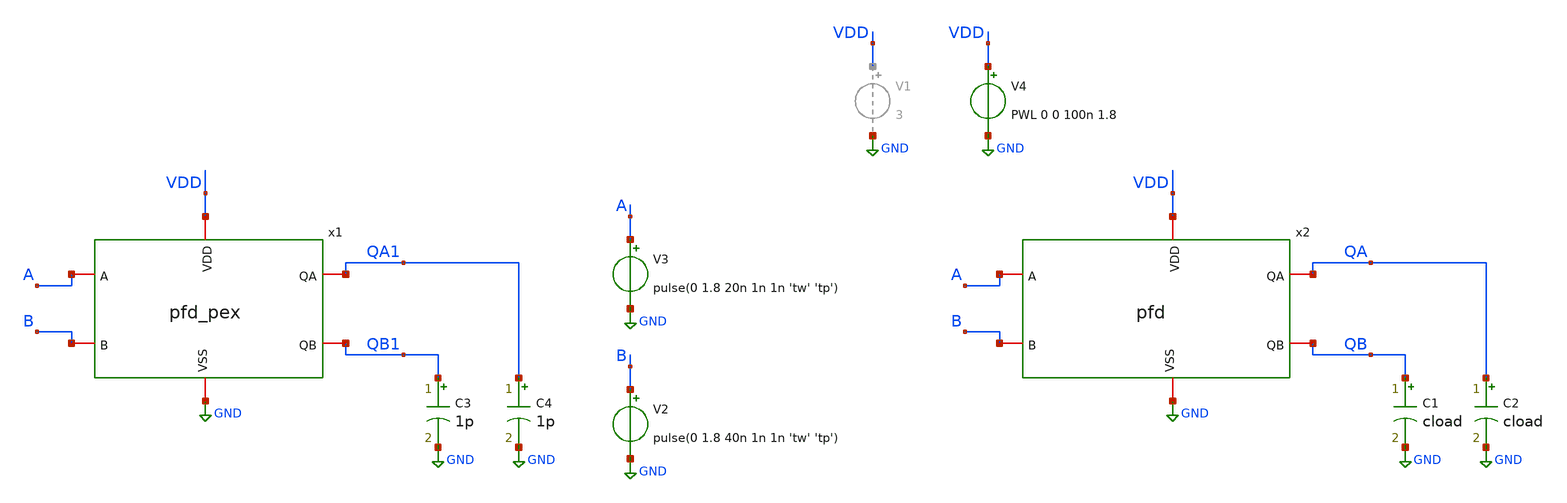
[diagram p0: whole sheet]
** sch_path: xschem/pfd/pfd_tran.sch
**.subckt pfd_tran
V2 B GND pulse(0 1.8 40n 1n 1n 'tw' 'tp')
V3 A GND pulse(0 1.8 20n 1n 1n 'tw' 'tp')
C1 QB GND cload m=1
C2 QA GND cload m=1
V4 VDD GND PWL 0 0 100n 1.8
C3 QB1 GND 1p m=1
C4 QA1 GND 1p m=1
x1 GND VDD A QA1 QB1 B pfd_pex
x2 GND VDD A QA QB B pfd
**** begin user architecture code


.options acct list
.temp 25
.param cload=500f  tw=40n tp=80n

.include /usr/local/share/pdk/sky130A/libs.ref/sky130_fd_sc_hd/spice/sky130_fd_sc_hd.spice

*.step cload 100f 500f 100f

.meas tran TRAN_PERIOD TRIG V(QA) VAL=0.5 RISE=1 TARG V(QA) VAL=0.5 RISE=2
.meas tran TRAN_FREQ param='1/TRAN_PERIOD'

.print TRAN_PERIOD  TRAN_FREQ

.control
save all
tran 0.1n 800n
step param R1 R1_start R1_stop R1_step
write pfd_tran.raw

.endc



** opencircuitdesign pdks install
.lib $::SKYWATER_MODELS/sky130.lib.spice tt


**** end user architecture code
**.ends

* expanding   symbol:  pfd/pfd_pex.sym # of pins=6
** sym_path: xschem/pfd/pfd.sym
.include [abs_sym_path pfd_pex.spice]

* expanding   symbol:  pfd/pfd.sym # of pins=6
** sym_path: xschem/pfd/pfd.sym
** sch_path: xschem/pfd/pfd.sch
.subckt pfd VSS VDD A QA QB B
*.iopin VDD
*.iopin A
*.iopin B
*.iopin QA
*.iopin QB
*.iopin VSS
x1 A VDD reset VSS VSS VDD VDD QA net2 sky130_fd_sc_hd__dfrbp_2
x2 QA QB VSS VSS VDD VDD net1 sky130_fd_sc_hd__and2_2
x3 B VDD reset VSS VSS VDD VDD QB net3 sky130_fd_sc_hd__dfrbp_2
x4 net1 VSS VSS VDD VDD reset sky130_fd_sc_hd__inv_4
.ends

.GLOBAL GND
.end
